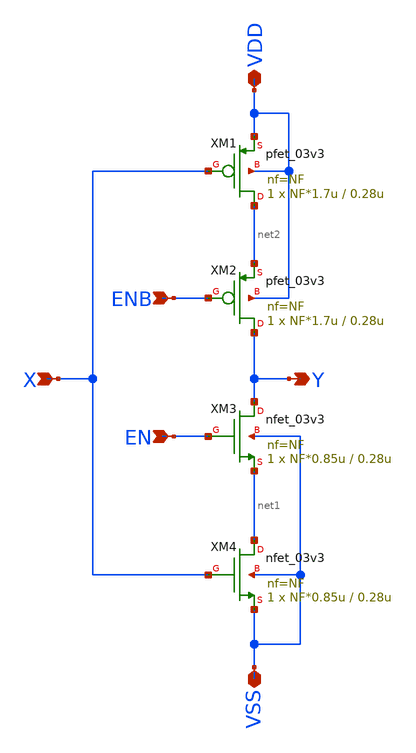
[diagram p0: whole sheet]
** sch_path: xschem_lib/DFFRAM_full_custom/tinv.sch
**.subckt tinv X ENB EN Y VDD VSS
*.ipin X
*.ipin ENB
*.ipin EN
*.opin Y
*.iopin VDD
*.iopin VSS
XM1 net2 X VDD VDD pfet_03v3 L=0.28u W=NF*1.7u nf=NF ad='int((nf+1)/2) * W/nf * 0.18u' as='int((nf+2)/2) * W/nf * 0.18u'
+ pd='2*int((nf+1)/2) * (W/nf + 0.18u)' ps='2*int((nf+2)/2) * (W/nf + 0.18u)' nrd='0.18u / W' nrs='0.18u / W'
+ sa=0 sb=0 sd=0 m=1
XM2 Y ENB net2 VDD pfet_03v3 L=0.28u W=NF*1.7u nf=NF ad='int((nf+1)/2) * W/nf * 0.18u' as='int((nf+2)/2) * W/nf * 0.18u'
+ pd='2*int((nf+1)/2) * (W/nf + 0.18u)' ps='2*int((nf+2)/2) * (W/nf + 0.18u)' nrd='0.18u / W' nrs='0.18u / W'
+ sa=0 sb=0 sd=0 m=1
XM3 Y EN net1 VSS nfet_03v3 L=0.28u W=NF*0.85u nf=NF ad='int((nf+1)/2) * W/nf * 0.18u' as='int((nf+2)/2) * W/nf * 0.18u'
+ pd='2*int((nf+1)/2) * (W/nf + 0.18u)' ps='2*int((nf+2)/2) * (W/nf + 0.18u)' nrd='0.18u / W' nrs='0.18u / W'
+ sa=0 sb=0 sd=0 m=1
XM4 net1 X VSS VSS nfet_03v3 L=0.28u W=NF*0.85u nf=NF ad='int((nf+1)/2) * W/nf * 0.18u' as='int((nf+2)/2) * W/nf * 0.18u'
+ pd='2*int((nf+1)/2) * (W/nf + 0.18u)' ps='2*int((nf+2)/2) * (W/nf + 0.18u)' nrd='0.18u / W' nrs='0.18u / W'
+ sa=0 sb=0 sd=0 m=1
**.ends
.end
